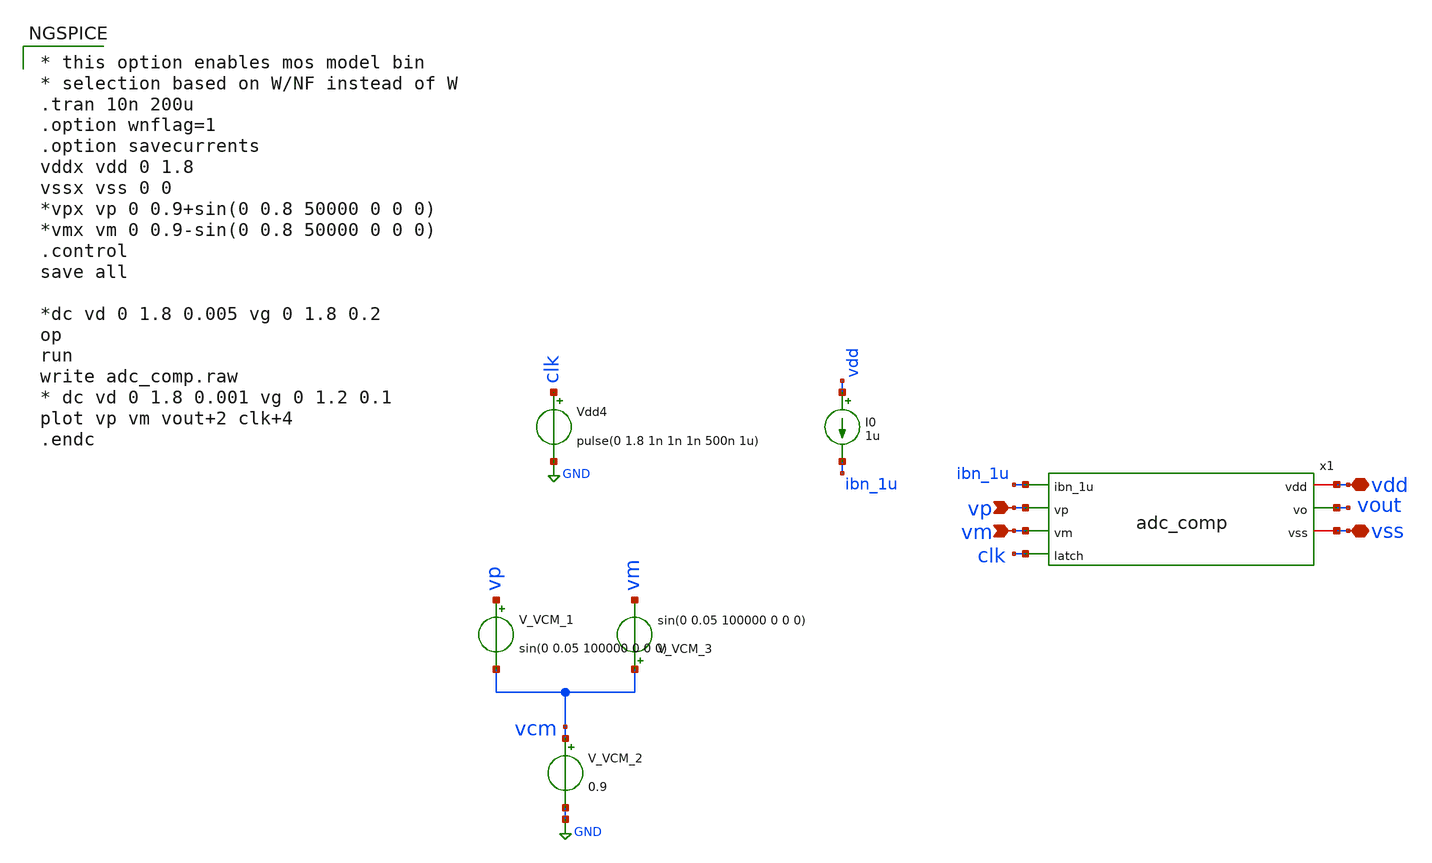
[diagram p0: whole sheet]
** sch_path: top/test/testbench/adc_comp_tb1.sch
.lib $::SKYWATER_MODELS/sky130.lib.spice tt
.include $::SKYWATER_STDCELLS/sky130_fd_sc_hd.spice

**.subckt adc_comp_tb1 vdd vss vp vm
*.iopin vdd
*.iopin vss
*.ipin vp
*.ipin vm
x1 vdd vout ibn_1u vp vm vss clk adc_comp
I0 vdd ibn_1u 1u
Vdd4 clk GND pulse(0 1.8 1n 1n 1n 500n 1u)
V_VCM_2 vcm GND 0.9
V_VCM_1 vp vcm sin(0 0.05 100000 0 0 0)
V_VCM_3 vcm vm sin(0 0.05 100000 0 0 0)
**** begin user architecture code

* this option enables mos model bin
* selection based on W/NF instead of W
.tran 10n 200u
.option wnflag=1
.option savecurrents
vddx vdd 0 1.8
vssx vss 0 0
*vpx vp 0 0.9+sin(0 0.8 50000 0 0 0)
*vmx vm 0 0.9-sin(0 0.8 50000 0 0 0)
.control
save all

*dc vd 0 1.8 0.005 vg 0 1.8 0.2
op
run
write adc_comp.raw
* dc vd 0 1.8 0.001 vg 0 1.2 0.1
plot vp vm vout+2 clk+4
.endc


**** end user architecture code
**.ends

* expanding   symbol:  /foss/designs/test/design/adc_comp.sym # of pins=7
** sym_path: test/design/adc_comp.sym
** sch_path: test/design/adc_comp.sch
.subckt adc_comp vdd vo ibn_1u vp vm vss latch
*.iopin vss
*.iopin vdd
*.ipin vp
*.ipin vm
*.ipin latch
*.ipin ibn_1u
*.opin vo
XM3 vom1 vp vx vss sky130_fd_pr__nfet_01v8_lvt L=1 W=2 nf=1 ad='int((nf+1)/2) * W/nf * 0.29' as='int((nf+2)/2) * W/nf * 0.29'
+ pd='2*int((nf+1)/2) * (W/nf + 0.29)' ps='2*int((nf+2)/2) * (W/nf + 0.29)' nrd='0.29 / W' nrs='0.29 / W'
+ sa=0 sb=0 sd=0 mult=8 m=8
XM4 vop1 vm vx vss sky130_fd_pr__nfet_01v8_lvt L=1 W=2 nf=1 ad='int((nf+1)/2) * W/nf * 0.29' as='int((nf+2)/2) * W/nf * 0.29'
+ pd='2*int((nf+1)/2) * (W/nf + 0.29)' ps='2*int((nf+2)/2) * (W/nf + 0.29)' nrd='0.29 / W' nrs='0.29 / W'
+ sa=0 sb=0 sd=0 mult=8 m=8
XM2 vop1 vbp vdd vdd sky130_fd_pr__pfet_01v8_lvt L=5 W=5 nf=1 ad='int((nf+1)/2) * W/nf * 0.29' as='int((nf+2)/2) * W/nf * 0.29'
+ pd='2*int((nf+1)/2) * (W/nf + 0.29)' ps='2*int((nf+2)/2) * (W/nf + 0.29)' nrd='0.29 / W' nrs='0.29 / W'
+ sa=0 sb=0 sd=0 mult=5 m=5
XM1 vom1 vbp vdd vdd sky130_fd_pr__pfet_01v8_lvt L=5 W=5 nf=1 ad='int((nf+1)/2) * W/nf * 0.29' as='int((nf+2)/2) * W/nf * 0.29'
+ pd='2*int((nf+1)/2) * (W/nf + 0.29)' ps='2*int((nf+2)/2) * (W/nf + 0.29)' nrd='0.29 / W' nrs='0.29 / W'
+ sa=0 sb=0 sd=0 mult=5 m=5
XM6 ibn_1u ibn_1u vss vss sky130_fd_pr__nfet_01v8 L=20 W=3 nf=1 ad='int((nf+1)/2) * W/nf * 0.29' as='int((nf+2)/2) * W/nf * 0.29'
+ pd='2*int((nf+1)/2) * (W/nf + 0.29)' ps='2*int((nf+2)/2) * (W/nf + 0.29)' nrd='0.29 / W' nrs='0.29 / W'
+ sa=0 sb=0 sd=0 mult=2 m=2
XM5 vx ibn_1u vss vss sky130_fd_pr__nfet_01v8 L=20 W=3 nf=1 ad='int((nf+1)/2) * W/nf * 0.29' as='int((nf+2)/2) * W/nf * 0.29'
+ pd='2*int((nf+1)/2) * (W/nf + 0.29)' ps='2*int((nf+2)/2) * (W/nf + 0.29)' nrd='0.29 / W' nrs='0.29 / W'
+ sa=0 sb=0 sd=0 mult=12 m=12
XM7 vbp ibn_1u vss vss sky130_fd_pr__nfet_01v8 L=20 W=3 nf=1 ad='int((nf+1)/2) * W/nf * 0.29' as='int((nf+2)/2) * W/nf * 0.29'
+ pd='2*int((nf+1)/2) * (W/nf + 0.29)' ps='2*int((nf+2)/2) * (W/nf + 0.29)' nrd='0.29 / W' nrs='0.29 / W'
+ sa=0 sb=0 sd=0 mult=1 m=1
XM8 vbp vbp vdd vdd sky130_fd_pr__pfet_01v8_lvt L=5 W=5 nf=1 ad='int((nf+1)/2) * W/nf * 0.29' as='int((nf+2)/2) * W/nf * 0.29'
+ pd='2*int((nf+1)/2) * (W/nf + 0.29)' ps='2*int((nf+2)/2) * (W/nf + 0.29)' nrd='0.29 / W' nrs='0.29 / W'
+ sa=0 sb=0 sd=0 mult=1 m=1
XM9 vx vop1 vdd vdd sky130_fd_pr__pfet_01v8_lvt L=1 W=5 nf=1 ad='int((nf+1)/2) * W/nf * 0.29' as='int((nf+2)/2) * W/nf * 0.29'
+ pd='2*int((nf+1)/2) * (W/nf + 0.29)' ps='2*int((nf+2)/2) * (W/nf + 0.29)' nrd='0.29 / W' nrs='0.29 / W'
+ sa=0 sb=0 sd=0 mult=2 m=2
XM10 vx vom1 vdd vdd sky130_fd_pr__pfet_01v8_lvt L=1 W=5 nf=1 ad='int((nf+1)/2) * W/nf * 0.29' as='int((nf+2)/2) * W/nf * 0.29'
+ pd='2*int((nf+1)/2) * (W/nf + 0.29)' ps='2*int((nf+2)/2) * (W/nf + 0.29)' nrd='0.29 / W' nrs='0.29 / W'
+ sa=0 sb=0 sd=0 mult=2 m=2
XM11 vop2 vom2 vss vss sky130_fd_pr__nfet_01v8 L=2 W=3 nf=1 ad='int((nf+1)/2) * W/nf * 0.29' as='int((nf+2)/2) * W/nf * 0.29'
+ pd='2*int((nf+1)/2) * (W/nf + 0.29)' ps='2*int((nf+2)/2) * (W/nf + 0.29)' nrd='0.29 / W' nrs='0.29 / W'
+ sa=0 sb=0 sd=0 mult=1 m=1
XM12 vom2 vop2 vss vss sky130_fd_pr__nfet_01v8 L=2 W=3 nf=1 ad='int((nf+1)/2) * W/nf * 0.29' as='int((nf+2)/2) * W/nf * 0.29'
+ pd='2*int((nf+1)/2) * (W/nf + 0.29)' ps='2*int((nf+2)/2) * (W/nf + 0.29)' nrd='0.29 / W' nrs='0.29 / W'
+ sa=0 sb=0 sd=0 mult=1 m=1
XM13 net4 vom1 vdd vdd sky130_fd_pr__pfet_01v8_lvt L=0.4 W=5 nf=1 ad='int((nf+1)/2) * W/nf * 0.29' as='int((nf+2)/2) * W/nf * 0.29'
+ pd='2*int((nf+1)/2) * (W/nf + 0.29)' ps='2*int((nf+2)/2) * (W/nf + 0.29)' nrd='0.29 / W' nrs='0.29 / W'
+ sa=0 sb=0 sd=0 mult=1 m=1
XM14 net3 vop1 vdd vdd sky130_fd_pr__pfet_01v8_lvt L=0.4 W=5 nf=1 ad='int((nf+1)/2) * W/nf * 0.29' as='int((nf+2)/2) * W/nf * 0.29'
+ pd='2*int((nf+1)/2) * (W/nf + 0.29)' ps='2*int((nf+2)/2) * (W/nf + 0.29)' nrd='0.29 / W' nrs='0.29 / W'
+ sa=0 sb=0 sd=0 mult=1 m=1
XM17 vom2 latch_n vss vss sky130_fd_pr__nfet_01v8 L=0.15 W=0.5 nf=1 ad='int((nf+1)/2) * W/nf * 0.29'
+ as='int((nf+2)/2) * W/nf * 0.29' pd='2*int((nf+1)/2) * (W/nf + 0.29)' ps='2*int((nf+2)/2) * (W/nf + 0.29)'
+ nrd='0.29 / W' nrs='0.29 / W' sa=0 sb=0 sd=0 mult=1 m=1
XM18 vop2 latch_n vss vss sky130_fd_pr__nfet_01v8 L=0.15 W=0.5 nf=1 ad='int((nf+1)/2) * W/nf * 0.29'
+ as='int((nf+2)/2) * W/nf * 0.29' pd='2*int((nf+1)/2) * (W/nf + 0.29)' ps='2*int((nf+2)/2) * (W/nf + 0.29)'
+ nrd='0.29 / W' nrs='0.29 / W' sa=0 sb=0 sd=0 mult=1 m=1
XM19 net1 vop2 vdd vdd sky130_fd_pr__pfet_01v8 L=0.15 W=1 nf=1 ad='int((nf+1)/2) * W/nf * 0.29' as='int((nf+2)/2) * W/nf * 0.29'
+ pd='2*int((nf+1)/2) * (W/nf + 0.29)' ps='2*int((nf+2)/2) * (W/nf + 0.29)' nrd='0.29 / W' nrs='0.29 / W'
+ sa=0 sb=0 sd=0 mult=1 m=1
XM20 net1 vop2 vss vss sky130_fd_pr__nfet_01v8 L=0.15 W=0.5 nf=1 ad='int((nf+1)/2) * W/nf * 0.29' as='int((nf+2)/2) * W/nf * 0.29'
+ pd='2*int((nf+1)/2) * (W/nf + 0.29)' ps='2*int((nf+2)/2) * (W/nf + 0.29)' nrd='0.29 / W' nrs='0.29 / W'
+ sa=0 sb=0 sd=0 mult=1 m=1
XM21 vo net1 vdd vdd sky130_fd_pr__pfet_01v8 L=0.15 W=1 nf=1 ad='int((nf+1)/2) * W/nf * 0.29' as='int((nf+2)/2) * W/nf * 0.29'
+ pd='2*int((nf+1)/2) * (W/nf + 0.29)' ps='2*int((nf+2)/2) * (W/nf + 0.29)' nrd='0.29 / W' nrs='0.29 / W'
+ sa=0 sb=0 sd=0 mult=2 m=2
XM22 vo net1 vss vss sky130_fd_pr__nfet_01v8 L=0.15 W=0.5 nf=1 ad='int((nf+1)/2) * W/nf * 0.29' as='int((nf+2)/2) * W/nf * 0.29'
+ pd='2*int((nf+1)/2) * (W/nf + 0.29)' ps='2*int((nf+2)/2) * (W/nf + 0.29)' nrd='0.29 / W' nrs='0.29 / W'
+ sa=0 sb=0 sd=0 mult=2 m=2
XM23 net2 vom2 vdd vdd sky130_fd_pr__pfet_01v8 L=0.15 W=1 nf=1 ad='int((nf+1)/2) * W/nf * 0.29' as='int((nf+2)/2) * W/nf * 0.29'
+ pd='2*int((nf+1)/2) * (W/nf + 0.29)' ps='2*int((nf+2)/2) * (W/nf + 0.29)' nrd='0.29 / W' nrs='0.29 / W'
+ sa=0 sb=0 sd=0 mult=1 m=1
XM24 net2 vom2 vss vss sky130_fd_pr__nfet_01v8 L=0.15 W=0.5 nf=1 ad='int((nf+1)/2) * W/nf * 0.29' as='int((nf+2)/2) * W/nf * 0.29'
+ pd='2*int((nf+1)/2) * (W/nf + 0.29)' ps='2*int((nf+2)/2) * (W/nf + 0.29)' nrd='0.29 / W' nrs='0.29 / W'
+ sa=0 sb=0 sd=0 mult=1 m=1
XM15 net5 vop2 net3 vdd sky130_fd_pr__pfet_01v8_lvt L=0.4 W=5 nf=1 ad='int((nf+1)/2) * W/nf * 0.29' as='int((nf+2)/2) * W/nf * 0.29'
+ pd='2*int((nf+1)/2) * (W/nf + 0.29)' ps='2*int((nf+2)/2) * (W/nf + 0.29)' nrd='0.29 / W' nrs='0.29 / W'
+ sa=0 sb=0 sd=0 mult=1 m=1
XM16 net6 vom2 net4 vdd sky130_fd_pr__pfet_01v8_lvt L=0.4 W=5 nf=1 ad='int((nf+1)/2) * W/nf * 0.29' as='int((nf+2)/2) * W/nf * 0.29'
+ pd='2*int((nf+1)/2) * (W/nf + 0.29)' ps='2*int((nf+2)/2) * (W/nf + 0.29)' nrd='0.29 / W' nrs='0.29 / W'
+ sa=0 sb=0 sd=0 mult=1 m=1
XM25 net5 latch vom2 vss sky130_fd_pr__nfet_01v8_lvt L=0.15 W=1 nf=1 ad='int((nf+1)/2) * W/nf * 0.29'
+ as='int((nf+2)/2) * W/nf * 0.29' pd='2*int((nf+1)/2) * (W/nf + 0.29)' ps='2*int((nf+2)/2) * (W/nf + 0.29)'
+ nrd='0.29 / W' nrs='0.29 / W' sa=0 sb=0 sd=0 mult=1 m=1
XM26 net6 latch vop2 vss sky130_fd_pr__nfet_01v8_lvt L=0.15 W=1 nf=1 ad='int((nf+1)/2) * W/nf * 0.29'
+ as='int((nf+2)/2) * W/nf * 0.29' pd='2*int((nf+1)/2) * (W/nf + 0.29)' ps='2*int((nf+2)/2) * (W/nf + 0.29)'
+ nrd='0.29 / W' nrs='0.29 / W' sa=0 sb=0 sd=0 mult=1 m=1
x30 latch vss vss vdd vdd latch_n sky130_fd_sc_hd__inv_1
XM27 vss ibn_1u vss vss sky130_fd_pr__nfet_01v8 L=20 W=3 nf=1 ad='int((nf+1)/2) * W/nf * 0.29' as='int((nf+2)/2) * W/nf * 0.29'
+ pd='2*int((nf+1)/2) * (W/nf + 0.29)' ps='2*int((nf+2)/2) * (W/nf + 0.29)' nrd='0.29 / W' nrs='0.29 / W'
+ sa=0 sb=0 sd=0 mult=2 m=2
XM28 vss vss vss vss sky130_fd_pr__nfet_01v8_lvt L=1 W=2 nf=1 ad='int((nf+1)/2) * W/nf * 0.29' as='int((nf+2)/2) * W/nf * 0.29'
+ pd='2*int((nf+1)/2) * (W/nf + 0.29)' ps='2*int((nf+2)/2) * (W/nf + 0.29)' nrd='0.29 / W' nrs='0.29 / W'
+ sa=0 sb=0 sd=0 mult=2 m=2
XM29 vss vss vss vss sky130_fd_pr__nfet_01v8_lvt L=1 W=1 nf=1 ad='int((nf+1)/2) * W/nf * 0.29' as='int((nf+2)/2) * W/nf * 0.29'
+ pd='2*int((nf+1)/2) * (W/nf + 0.29)' ps='2*int((nf+2)/2) * (W/nf + 0.29)' nrd='0.29 / W' nrs='0.29 / W'
+ sa=0 sb=0 sd=0 mult=20 m=20
XM30 vdd vbp vdd vdd sky130_fd_pr__pfet_01v8_lvt L=5 W=5 nf=1 ad='int((nf+1)/2) * W/nf * 0.29' as='int((nf+2)/2) * W/nf * 0.29'
+ pd='2*int((nf+1)/2) * (W/nf + 0.29)' ps='2*int((nf+2)/2) * (W/nf + 0.29)' nrd='0.29 / W' nrs='0.29 / W'
+ sa=0 sb=0 sd=0 mult=2 m=2
XM31 vdd vdd vdd vdd sky130_fd_pr__pfet_01v8_lvt L=1 W=5 nf=1 ad='int((nf+1)/2) * W/nf * 0.29' as='int((nf+2)/2) * W/nf * 0.29'
+ pd='2*int((nf+1)/2) * (W/nf + 0.29)' ps='2*int((nf+2)/2) * (W/nf + 0.29)' nrd='0.29 / W' nrs='0.29 / W'
+ sa=0 sb=0 sd=0 mult=2 m=2
.ends

.GLOBAL GND
.end
